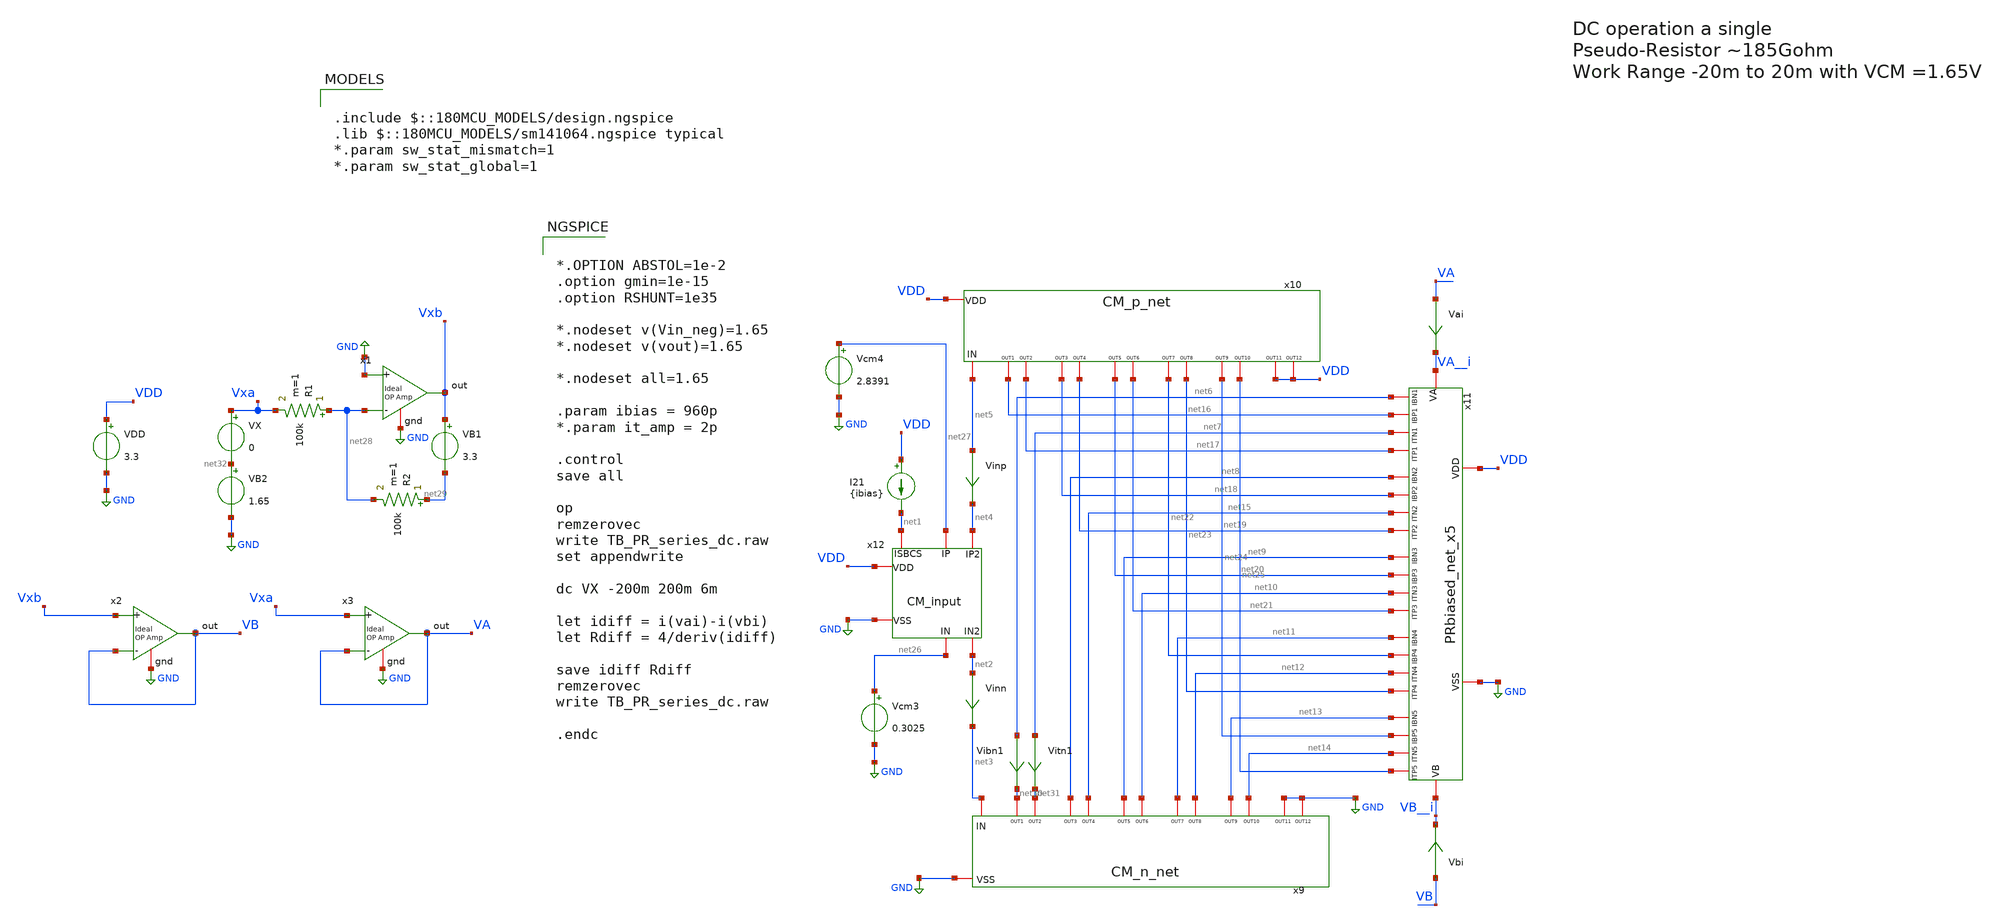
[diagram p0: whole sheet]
** sch_path: TIA_Filter/PseudoResistor/TB_PR_series_dc.sch
**.subckt TB_PR_series_dc
x9 net3 net30 net31 net8 net15 net9 net10 net11 net12 net13 net14 GND GND GND CM_n_net
x10 net5 net16 net17 net18 net19 net20 net21 net22 net23 net24 net25 VDD VDD VDD CM_p_net
x11 VA__i VB__i net9 net8 net6 net13 net11 net20 net18 net22 net16 net24 net10 net7 net14 net15
+ net12 net25 net19 net17 net23 net21 VDD GND PRbiased_net_x5
x12 net27 net4 net26 net2 net1 VDD GND CM_input
I21 VDD net1 {ibias}
Vai VA VA__i 0
.save i(vai)
Vbi VB VB__i 0
.save i(vbi)
Vinn net2 net3 0
.save i(vinn)
Vinp net5 net4 0
.save i(vinp)
Vcm3 net26 GND 0.3025
Vcm4 net27 GND 2.8391
VDD VDD GND 3.3
VX Vxa net32 0
VB1 Vxb net29 3.3
R1 net28 Vxa 100k m=1
R2 net29 net28 100k m=1
VB2 net32 GND 1.65
x2 VB Vxb VB GND ampOp_ideal
x3 VA Vxa VA GND ampOp_ideal
x1 Vxb GND net28 GND ampOp_ideal
Vibn1 net6 net30 0
.save i(vibn1)
Vitn1 net7 net31 0
.save i(vitn1)
**** begin user architecture code

.include $::180MCU_MODELS/design.ngspice
.lib $::180MCU_MODELS/sm141064.ngspice typical
*.param sw_stat_mismatch=1
*.param sw_stat_global=1



*.OPTION ABSTOL=1e-2
.option gmin=1e-15
.option RSHUNT=1e35

*.nodeset v(Vin_neg)=1.65
*.nodeset v(vout)=1.65

*.nodeset all=1.65

.param ibias = 960p
*.param it_amp = 2p

.control
save all

op
remzerovec
write TB_PR_series_dc.raw
set appendwrite

dc VX -200m 200m 6m

let idiff = i(vai)-i(vbi)
let Rdiff = 4/deriv(idiff)

save idiff Rdiff
remzerovec
write TB_PR_series_dc.raw

.endc


**** end user architecture code
**.ends
.GLOBAL GND
.end
